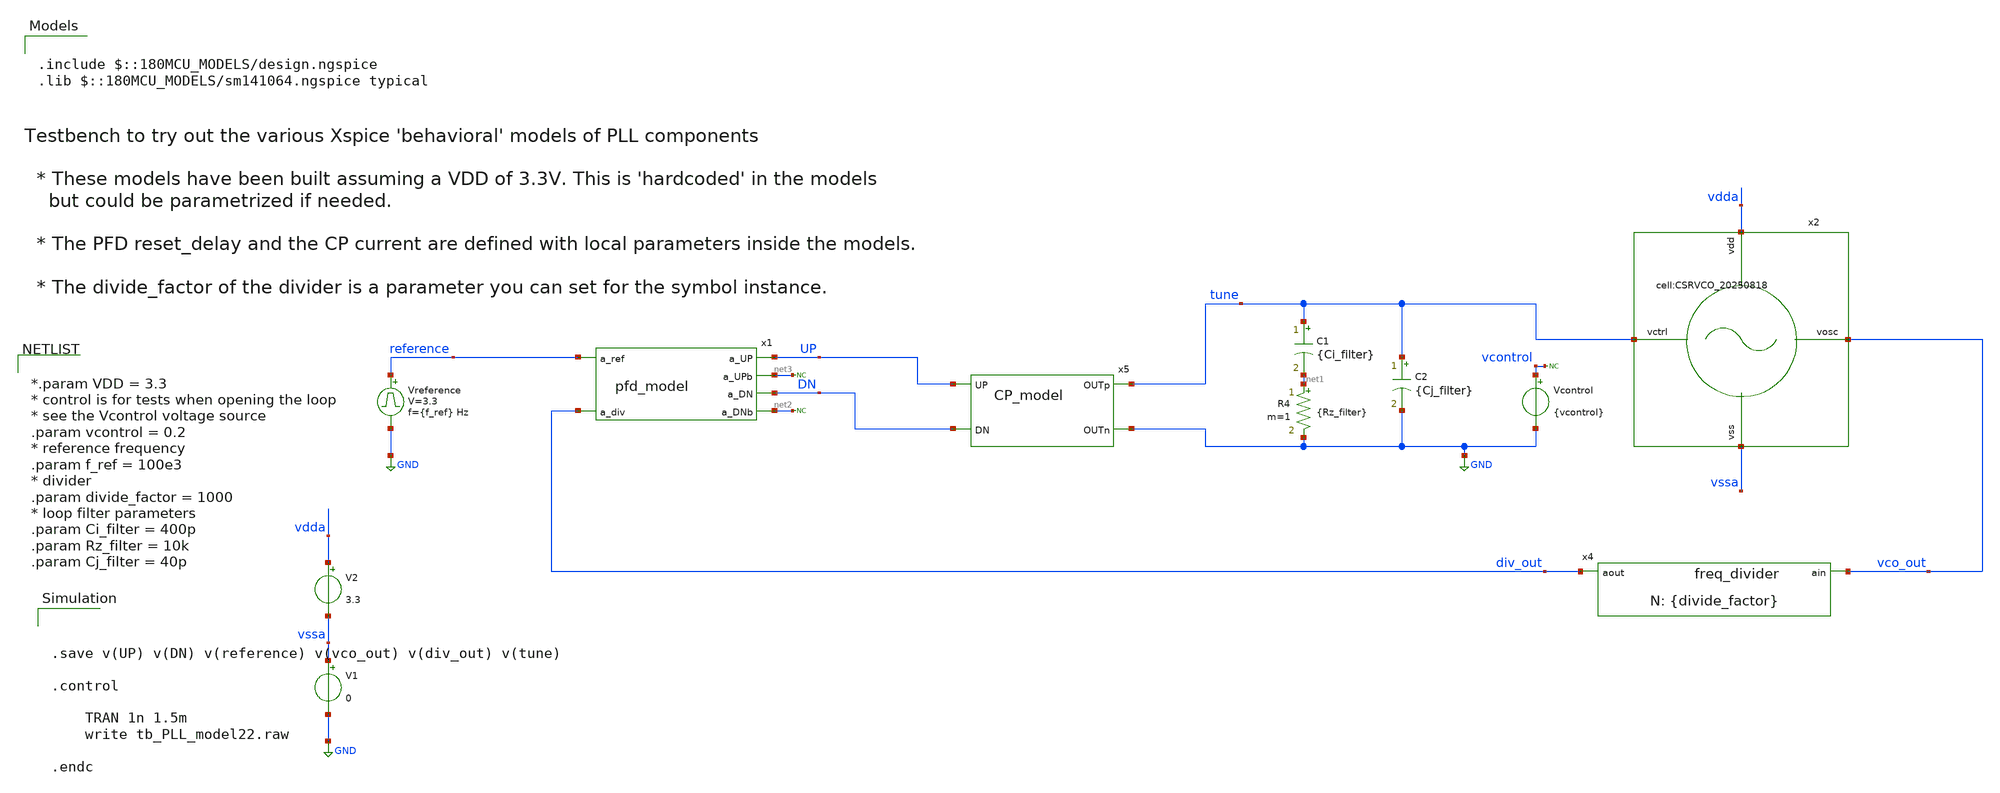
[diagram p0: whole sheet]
** sch_path: designs/libs/tb_pll/tb_PLL_VCO.sch
**.subckt tb_PLL_VCO
Vcontrol vcontrol GND {vcontrol}
Vreference reference GND pulse 0 3.3 '0.495/ {f_ref} ' '0.01/{f_ref} ' '0.01/{f_ref} ' '0.49/{f_ref} '
+ '1/{f_ref} '
C1 tune net1 {Ci_filter} m=1
R4 net1 GND {Rz_filter} m=1
* noconn vcontrol
C2 tune GND {Cj_filter} m=1
x4 div_out vco_out freq_divider divide_factor={divide_factor}
V1 vssa GND 0
V2 vdda vssa 3.3
* noconn #net3
x1 reference UP net3 DN div_out net2 pfd_model
* noconn #net2
x5 tune UP DN GND CP_model
x2 tune vdda vssa vco_out CSRVCO_20250818
**** begin user architecture code



.save v(UP) v(DN) v(reference) v(vco_out) v(div_out) v(tune)

.control

    TRAN 1n 1.5m
    write tb_PLL_model22.raw

.endc




*.param VDD = 3.3
* control is for tests when opening the loop
* see the Vcontrol voltage source
.param vcontrol = 0.2
* reference frequency
.param f_ref = 100e3
* divider
.param divide_factor = 1000
* loop filter parameters
.param Ci_filter = 400p
.param Rz_filter = 10k
.param Cj_filter = 40p



.include $::180MCU_MODELS/design.ngspice
.lib $::180MCU_MODELS/sm141064.ngspice typical

**** end user architecture code
**.ends
.GLOBAL GND
.end
